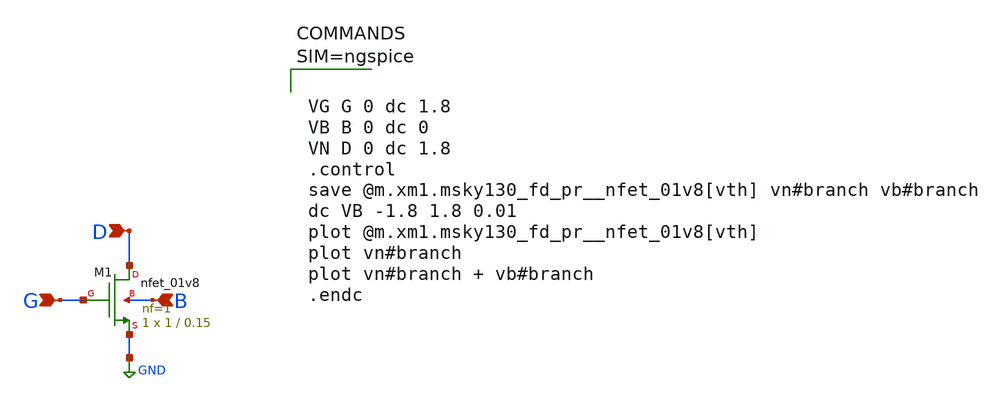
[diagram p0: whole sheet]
** sch_path: trbench_body.sch
**.subckt trbench_body D G B
*.ipin D
*.ipin G
*.ipin B
XM1 D G GND B sky130_fd_pr__nfet_01v8 L=0.15 W=1 nf=1 ad='int((nf+1)/2) * W/nf * 0.29' as='int((nf+2)/2) * W/nf * 0.29'
+ pd='2*int((nf+1)/2) * (W/nf + 0.29)' ps='2*int((nf+2)/2) * (W/nf + 0.29)' nrd='0.29 / W' nrs='0.29 / W'
+ sa=0 sb=0 sd=0 mult=1 m=1
**** begin user architecture code



VG G 0 dc 1.8
VB B 0 dc 0
VN D 0 dc 1.8
.control
save @m.xm1.msky130_fd_pr__nfet_01v8[vth] vn#branch vb#branch
dc VB -1.8 1.8 0.01
plot @m.xm1.msky130_fd_pr__nfet_01v8[vth]
plot vn#branch
plot vn#branch + vb#branch
.endc



 .param mc_mm_switch=0
.param mc_pr_switch=0
.include $::SKYWATER_MODELS/corners/tt.spice
.include $::SKYWATER_MODELS/r+c/res_typical__cap_typical.spice
.include $::SKYWATER_MODELS/r+c/res_typical__cap_typical__lin.spice
.include $::SKYWATER_MODELS/corners/tt/specialized_cells.spice
.include $::SKYWATER_STDCELLS/sky130_fd_sc_hd.spice

**** end user architecture code
**.ends
.GLOBAL GND
.end
